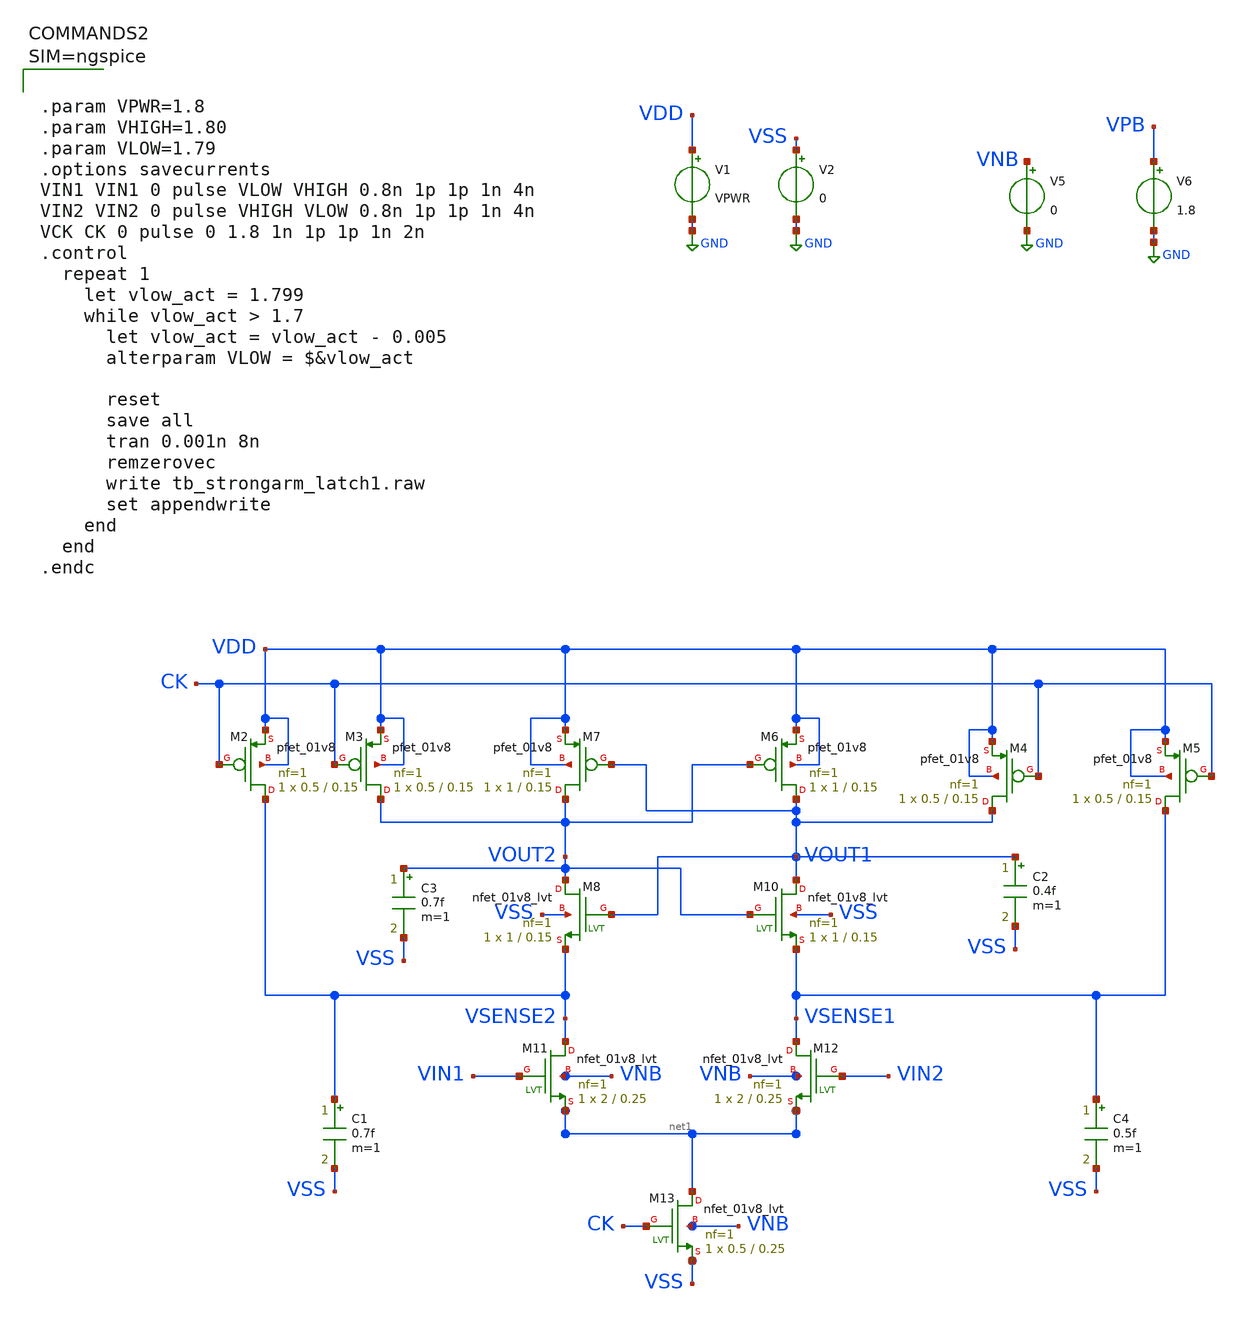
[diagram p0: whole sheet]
** sch_path: xschem/tb_strongarm_latch1.sch
**.subckt tb_strongarm_latch1
V5 VNB GND 0
V6 VPB GND 1.8
V2 VSS GND 0
V1 VDD GND VPWR
XM8 VOUT2 VOUT1 VSENSE2 VSS sky130_fd_pr__nfet_01v8_lvt L=0.15 W=1 nf=1 ad='int((nf+1)/2) * W/nf * 0.29'
+ as='int((nf+2)/2) * W/nf * 0.29' pd='2*int((nf+1)/2) * (W/nf + 0.29)' ps='2*int((nf+2)/2) * (W/nf + 0.29)'
+ nrd='0.29 / W' nrs='0.29 / W' sa=0 sb=0 sd=0 mult=1 m=1
XM10 VOUT1 VOUT2 VSENSE1 VSS sky130_fd_pr__nfet_01v8_lvt L=0.15 W=1 nf=1 ad='int((nf+1)/2) * W/nf * 0.29'
+ as='int((nf+2)/2) * W/nf * 0.29' pd='2*int((nf+1)/2) * (W/nf + 0.29)' ps='2*int((nf+2)/2) * (W/nf + 0.29)'
+ nrd='0.29 / W' nrs='0.29 / W' sa=0 sb=0 sd=0 mult=1 m=1
XM11 VSENSE2 VIN1 net1 VNB sky130_fd_pr__nfet_01v8_lvt L=0.25 W=2 nf=1 ad='int((nf+1)/2) * W/nf * 0.29'
+ as='int((nf+2)/2) * W/nf * 0.29' pd='2*int((nf+1)/2) * (W/nf + 0.29)' ps='2*int((nf+2)/2) * (W/nf + 0.29)'
+ nrd='0.29 / W' nrs='0.29 / W' sa=0 sb=0 sd=0 mult=1 m=1
XM12 VSENSE1 VIN2 net1 VNB sky130_fd_pr__nfet_01v8_lvt L=0.25 W=2 nf=1 ad='int((nf+1)/2) * W/nf * 0.29'
+ as='int((nf+2)/2) * W/nf * 0.29' pd='2*int((nf+1)/2) * (W/nf + 0.29)' ps='2*int((nf+2)/2) * (W/nf + 0.29)'
+ nrd='0.29 / W' nrs='0.29 / W' sa=0 sb=0 sd=0 mult=1 m=1
XM13 net1 CK VSS VNB sky130_fd_pr__nfet_01v8_lvt L=0.25 W=0.5 nf=1 ad='int((nf+1)/2) * W/nf * 0.29' as='int((nf+2)/2) * W/nf * 0.29'
+ pd='2*int((nf+1)/2) * (W/nf + 0.29)' ps='2*int((nf+2)/2) * (W/nf + 0.29)' nrd='0.29 / W' nrs='0.29 / W'
+ sa=0 sb=0 sd=0 mult=1 m=1
C4 VSENSE1 VSS 0.5f m=1
C1 VSENSE2 VSS 0.7f m=1
XM2 VSENSE2 CK VDD VDD sky130_fd_pr__pfet_01v8 L=0.15 W=0.5 nf=1 ad='int((nf+1)/2) * W/nf * 0.29' as='int((nf+2)/2) * W/nf * 0.29'
+ pd='2*int((nf+1)/2) * (W/nf + 0.29)' ps='2*int((nf+2)/2) * (W/nf + 0.29)' nrd='0.29 / W' nrs='0.29 / W'
+ sa=0 sb=0 sd=0 mult=1 m=1
XM3 VOUT2 CK VDD VDD sky130_fd_pr__pfet_01v8 L=0.15 W=0.5 nf=1 ad='int((nf+1)/2) * W/nf * 0.29' as='int((nf+2)/2) * W/nf * 0.29'
+ pd='2*int((nf+1)/2) * (W/nf + 0.29)' ps='2*int((nf+2)/2) * (W/nf + 0.29)' nrd='0.29 / W' nrs='0.29 / W'
+ sa=0 sb=0 sd=0 mult=1 m=1
XM4 VOUT1 CK VDD VDD sky130_fd_pr__pfet_01v8 L=0.15 W=0.5 nf=1 ad='int((nf+1)/2) * W/nf * 0.29' as='int((nf+2)/2) * W/nf * 0.29'
+ pd='2*int((nf+1)/2) * (W/nf + 0.29)' ps='2*int((nf+2)/2) * (W/nf + 0.29)' nrd='0.29 / W' nrs='0.29 / W'
+ sa=0 sb=0 sd=0 mult=1 m=1
XM5 VSENSE1 CK VDD VDD sky130_fd_pr__pfet_01v8 L=0.15 W=0.5 nf=1 ad='int((nf+1)/2) * W/nf * 0.29' as='int((nf+2)/2) * W/nf * 0.29'
+ pd='2*int((nf+1)/2) * (W/nf + 0.29)' ps='2*int((nf+2)/2) * (W/nf + 0.29)' nrd='0.29 / W' nrs='0.29 / W'
+ sa=0 sb=0 sd=0 mult=1 m=1
XM6 VOUT1 VOUT2 VDD VDD sky130_fd_pr__pfet_01v8 L=0.15 W=1 nf=1 ad='int((nf+1)/2) * W/nf * 0.29' as='int((nf+2)/2) * W/nf * 0.29'
+ pd='2*int((nf+1)/2) * (W/nf + 0.29)' ps='2*int((nf+2)/2) * (W/nf + 0.29)' nrd='0.29 / W' nrs='0.29 / W'
+ sa=0 sb=0 sd=0 mult=1 m=1
XM7 VOUT2 VOUT1 VDD VDD sky130_fd_pr__pfet_01v8 L=0.15 W=1 nf=1 ad='int((nf+1)/2) * W/nf * 0.29' as='int((nf+2)/2) * W/nf * 0.29'
+ pd='2*int((nf+1)/2) * (W/nf + 0.29)' ps='2*int((nf+2)/2) * (W/nf + 0.29)' nrd='0.29 / W' nrs='0.29 / W'
+ sa=0 sb=0 sd=0 mult=1 m=1
C2 VOUT1 VSS 0.4f m=1
C3 VOUT2 VSS 0.7f m=1
**** begin user architecture code

** opencircuitdesign pdks install
.lib $::SKYWATER_MODELS/sky130.lib.spice tt_mm
*.lib $::SKYWATER_STDCELLS/sky130_fd_sc_hd_blablabla.spice

.subckt sky130_fd_sc_hd__inv_1 A VGND VNB VPB VPWR Y
X0 VGND A Y VNB sky130_fd_pr__nfet_01v8 w=650000u l=150000u
X1 VPWR A Y VPB sky130_fd_pr__pfet_01v8_hvt w=1e+06u l=150000u
.ends





.param VPWR=1.8
.param VHIGH=1.80
.param VLOW=1.79
.options savecurrents
VIN1 VIN1 0 pulse VLOW VHIGH 0.8n 1p 1p 1n 4n
VIN2 VIN2 0 pulse VHIGH VLOW 0.8n 1p 1p 1n 4n
VCK CK 0 pulse 0 1.8 1n 1p 1p 1n 2n
.control
  repeat 1
    let vlow_act = 1.799
    while vlow_act > 1.7
      let vlow_act = vlow_act - 0.005
      alterparam VLOW = $&vlow_act

      reset
      save all
      tran 0.001n 8n
      remzerovec
      write tb_strongarm_latch1.raw
      set appendwrite
    end
  end
.endc



**** end user architecture code
**.ends
.GLOBAL GND
.end
